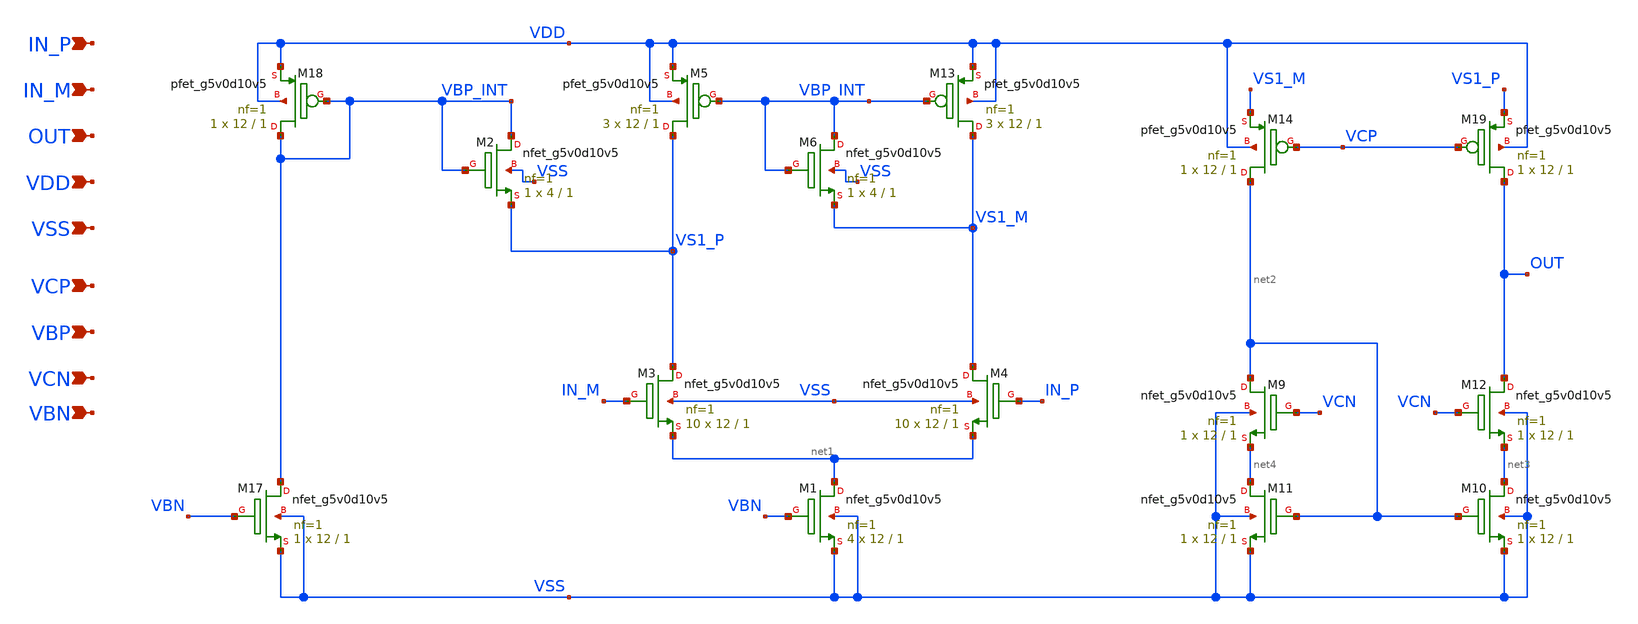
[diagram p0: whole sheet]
** sch_path: design/folded-cascode-n-in/folded_cascode_n_in.sch
**.subckt folded_cascode_n_in IN_P IN_M OUT VDD VSS VCP VBP VCN VBN
*.ipin IN_P
*.ipin IN_M
*.ipin OUT
*.ipin VDD
*.ipin VSS
*.ipin VCP
*.ipin VBP
*.ipin VCN
*.ipin VBN
XM1 net1 VBN VSS VSS sky130_fd_pr__nfet_g5v0d10v5 L=1 W=12 nf=1 ad='int((nf+1)/2) * W/nf * 0.29' as='int((nf+2)/2) * W/nf * 0.29'
+ pd='2*int((nf+1)/2) * (W/nf + 0.29)' ps='2*int((nf+2)/2) * (W/nf + 0.29)' nrd='0.29 / W' nrs='0.29 / W'
+ sa=0 sb=0 sd=0 mult=4 m=4
XM3 VS1_P IN_M net1 VSS sky130_fd_pr__nfet_g5v0d10v5 L=1 W=12 nf=1 ad='int((nf+1)/2) * W/nf * 0.29' as='int((nf+2)/2) * W/nf * 0.29'
+ pd='2*int((nf+1)/2) * (W/nf + 0.29)' ps='2*int((nf+2)/2) * (W/nf + 0.29)' nrd='0.29 / W' nrs='0.29 / W'
+ sa=0 sb=0 sd=0 mult=10 m=10
XM4 VS1_M IN_P net1 VSS sky130_fd_pr__nfet_g5v0d10v5 L=1 W=12 nf=1 ad='int((nf+1)/2) * W/nf * 0.29' as='int((nf+2)/2) * W/nf * 0.29'
+ pd='2*int((nf+1)/2) * (W/nf + 0.29)' ps='2*int((nf+2)/2) * (W/nf + 0.29)' nrd='0.29 / W' nrs='0.29 / W'
+ sa=0 sb=0 sd=0 mult=10 m=10
XM9 net2 VCN net4 VSS sky130_fd_pr__nfet_g5v0d10v5 L=1 W=12 nf=1 ad='int((nf+1)/2) * W/nf * 0.29' as='int((nf+2)/2) * W/nf * 0.29'
+ pd='2*int((nf+1)/2) * (W/nf + 0.29)' ps='2*int((nf+2)/2) * (W/nf + 0.29)' nrd='0.29 / W' nrs='0.29 / W'
+ sa=0 sb=0 sd=0 mult=1 m=1
XM10 net3 net2 VSS VSS sky130_fd_pr__nfet_g5v0d10v5 L=1 W=12 nf=1 ad='int((nf+1)/2) * W/nf * 0.29' as='int((nf+2)/2) * W/nf * 0.29'
+ pd='2*int((nf+1)/2) * (W/nf + 0.29)' ps='2*int((nf+2)/2) * (W/nf + 0.29)' nrd='0.29 / W' nrs='0.29 / W'
+ sa=0 sb=0 sd=0 mult=1 m=1
XM11 net4 net2 VSS VSS sky130_fd_pr__nfet_g5v0d10v5 L=1 W=12 nf=1 ad='int((nf+1)/2) * W/nf * 0.29' as='int((nf+2)/2) * W/nf * 0.29'
+ pd='2*int((nf+1)/2) * (W/nf + 0.29)' ps='2*int((nf+2)/2) * (W/nf + 0.29)' nrd='0.29 / W' nrs='0.29 / W'
+ sa=0 sb=0 sd=0 mult=1 m=1
XM12 OUT VCN net3 VSS sky130_fd_pr__nfet_g5v0d10v5 L=1 W=12 nf=1 ad='int((nf+1)/2) * W/nf * 0.29' as='int((nf+2)/2) * W/nf * 0.29'
+ pd='2*int((nf+1)/2) * (W/nf + 0.29)' ps='2*int((nf+2)/2) * (W/nf + 0.29)' nrd='0.29 / W' nrs='0.29 / W'
+ sa=0 sb=0 sd=0 mult=1 m=1
XM5 VS1_P VBP_INT VDD VDD sky130_fd_pr__pfet_g5v0d10v5 L=1 W=12 nf=1 ad='int((nf+1)/2) * W/nf * 0.29'
+ as='int((nf+2)/2) * W/nf * 0.29' pd='2*int((nf+1)/2) * (W/nf + 0.29)' ps='2*int((nf+2)/2) * (W/nf + 0.29)'
+ nrd='0.29 / W' nrs='0.29 / W' sa=0 sb=0 sd=0 mult=3 m=3
XM13 VS1_M VBP_INT VDD VDD sky130_fd_pr__pfet_g5v0d10v5 L=1 W=12 nf=1 ad='int((nf+1)/2) * W/nf * 0.29'
+ as='int((nf+2)/2) * W/nf * 0.29' pd='2*int((nf+1)/2) * (W/nf + 0.29)' ps='2*int((nf+2)/2) * (W/nf + 0.29)'
+ nrd='0.29 / W' nrs='0.29 / W' sa=0 sb=0 sd=0 mult=3 m=3
XM17 VBP_INT VBN VSS VSS sky130_fd_pr__nfet_g5v0d10v5 L=1 W=12 nf=1 ad='int((nf+1)/2) * W/nf * 0.29'
+ as='int((nf+2)/2) * W/nf * 0.29' pd='2*int((nf+1)/2) * (W/nf + 0.29)' ps='2*int((nf+2)/2) * (W/nf + 0.29)'
+ nrd='0.29 / W' nrs='0.29 / W' sa=0 sb=0 sd=0 mult=1 m=1
XM18 VBP_INT VBP_INT VDD VDD sky130_fd_pr__pfet_g5v0d10v5 L=1 W=12 nf=1 ad='int((nf+1)/2) * W/nf * 0.29'
+ as='int((nf+2)/2) * W/nf * 0.29' pd='2*int((nf+1)/2) * (W/nf + 0.29)' ps='2*int((nf+2)/2) * (W/nf + 0.29)'
+ nrd='0.29 / W' nrs='0.29 / W' sa=0 sb=0 sd=0 mult=1 m=1
XM14 net2 VCP VS1_M VDD sky130_fd_pr__pfet_g5v0d10v5 L=1 W=12 nf=1 ad='int((nf+1)/2) * W/nf * 0.29' as='int((nf+2)/2) * W/nf * 0.29'
+ pd='2*int((nf+1)/2) * (W/nf + 0.29)' ps='2*int((nf+2)/2) * (W/nf + 0.29)' nrd='0.29 / W' nrs='0.29 / W'
+ sa=0 sb=0 sd=0 mult=1 m=1
XM19 OUT VCP VS1_P VDD sky130_fd_pr__pfet_g5v0d10v5 L=1 W=12 nf=1 ad='int((nf+1)/2) * W/nf * 0.29' as='int((nf+2)/2) * W/nf * 0.29'
+ pd='2*int((nf+1)/2) * (W/nf + 0.29)' ps='2*int((nf+2)/2) * (W/nf + 0.29)' nrd='0.29 / W' nrs='0.29 / W'
+ sa=0 sb=0 sd=0 mult=1 m=1
XM2 VBP_INT VBP_INT VS1_P VSS sky130_fd_pr__nfet_g5v0d10v5 L=1 W=4 nf=1 ad='int((nf+1)/2) * W/nf * 0.29'
+ as='int((nf+2)/2) * W/nf * 0.29' pd='2*int((nf+1)/2) * (W/nf + 0.29)' ps='2*int((nf+2)/2) * (W/nf + 0.29)'
+ nrd='0.29 / W' nrs='0.29 / W' sa=0 sb=0 sd=0 mult=1 m=1
XM6 VBP_INT VBP_INT VS1_M VSS sky130_fd_pr__nfet_g5v0d10v5 L=1 W=4 nf=1 ad='int((nf+1)/2) * W/nf * 0.29'
+ as='int((nf+2)/2) * W/nf * 0.29' pd='2*int((nf+1)/2) * (W/nf + 0.29)' ps='2*int((nf+2)/2) * (W/nf + 0.29)'
+ nrd='0.29 / W' nrs='0.29 / W' sa=0 sb=0 sd=0 mult=1 m=1
**.ends
.end
